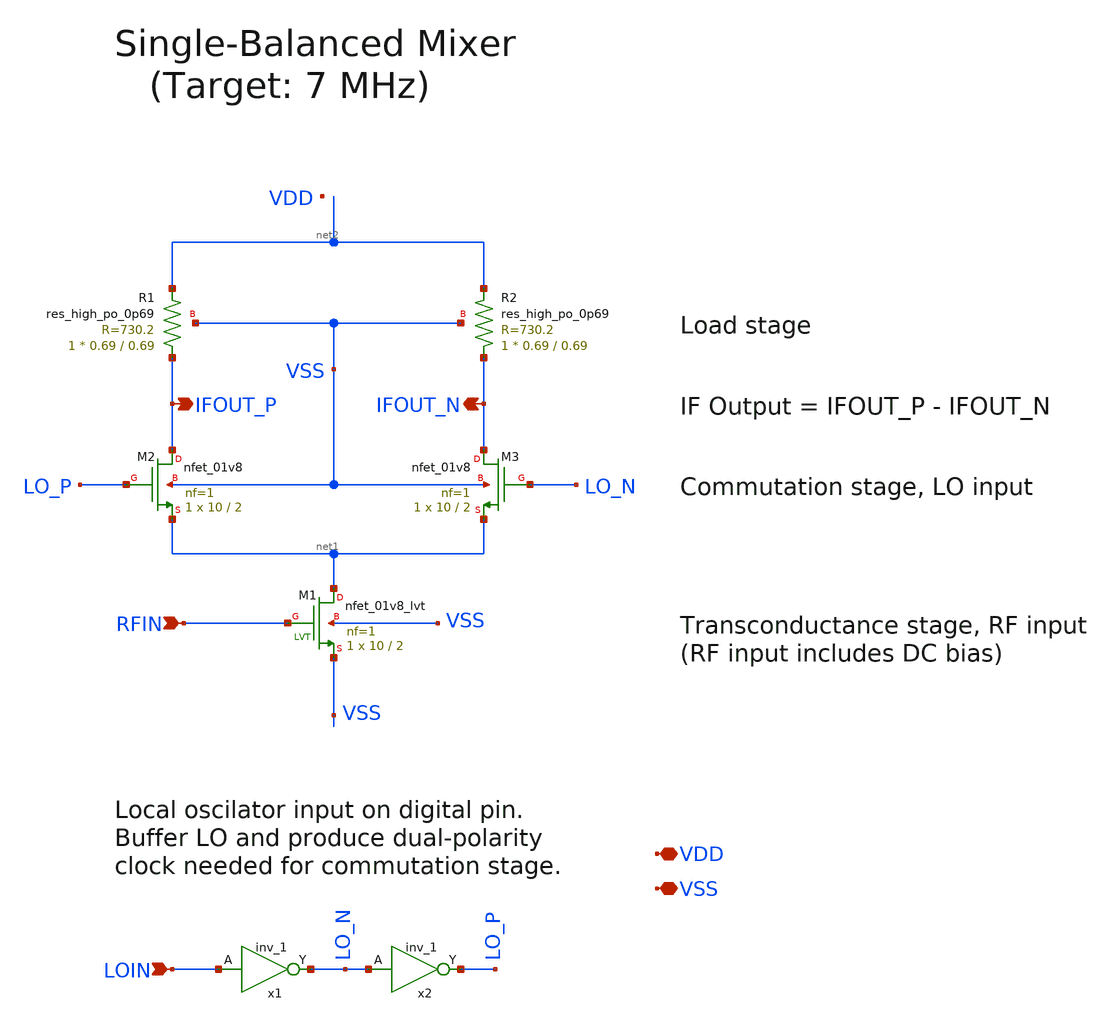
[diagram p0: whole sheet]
** sch_path: xschem/sb_mixer.sch
**.subckt sb_mixer VDD VSS LOIN RFIN IFOUT_P IFOUT_N
*.iopin VDD
*.iopin VSS
*.ipin LOIN
*.ipin RFIN
*.opin IFOUT_P
*.opin IFOUT_N
x1 LOIN VGND VNB VPB VPWR LO_N sky130_fd_sc_hd__inv_1
x2 LO_N VGND VNB VPB VPWR LO_P sky130_fd_sc_hd__inv_1
XM1 net1 RFIN VSS VSS sky130_fd_pr__nfet_01v8_lvt L=2 W=10 nf=1 ad='int((nf+1)/2) * W/nf * 0.29' as='int((nf+2)/2) * W/nf * 0.29'
+ pd='2*int((nf+1)/2) * (W/nf + 0.29)' ps='2*int((nf+2)/2) * (W/nf + 0.29)' nrd='0.29 / W' nrs='0.29 / W'
+ sa=0 sb=0 sd=0 mult=1 m=1
XM2 IFOUT_P LO_P net1 VSS sky130_fd_pr__nfet_01v8 L=2 W=10 nf=1 ad='int((nf+1)/2) * W/nf * 0.29' as='int((nf+2)/2) * W/nf * 0.29'
+ pd='2*int((nf+1)/2) * (W/nf + 0.29)' ps='2*int((nf+2)/2) * (W/nf + 0.29)' nrd='0.29 / W' nrs='0.29 / W'
+ sa=0 sb=0 sd=0 mult=1 m=1
XM3 IFOUT_N LO_N net1 VSS sky130_fd_pr__nfet_01v8 L=2 W=10 nf=1 ad='int((nf+1)/2) * W/nf * 0.29' as='int((nf+2)/2) * W/nf * 0.29'
+ pd='2*int((nf+1)/2) * (W/nf + 0.29)' ps='2*int((nf+2)/2) * (W/nf + 0.29)' nrd='0.29 / W' nrs='0.29 / W'
+ sa=0 sb=0 sd=0 mult=1 m=1
XR1 IFOUT_P net2 VSS sky130_fd_pr__res_high_po_0p69 L=0.69 mult=1 m=1
XR2 IFOUT_N net2 VSS sky130_fd_pr__res_high_po_0p69 L=0.69 mult=1 m=1
**.ends
.end
